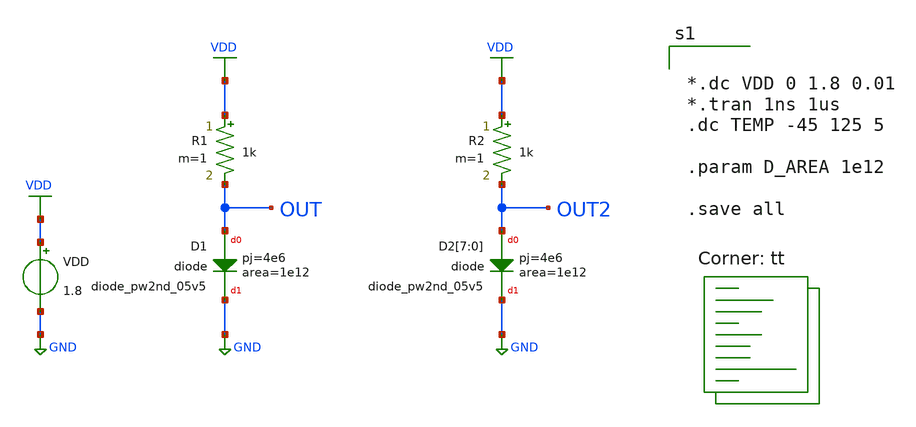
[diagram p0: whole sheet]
** sch_path: design/CNR_GR04_SKY130NM/CNR_GR4_Temp_Sweep_PK.sch
**.subckt CNR_GR4_Temp_Sweep_PK
XD1 OUT GND sky130_fd_pr__diode_pw2nd_05v5 area=1e12 pj=4e6
R1 VDD OUT 1k m=1
VDD VDD GND 1.8
XD2[7] OUT2 GND sky130_fd_pr__diode_pw2nd_05v5 area=1e12 pj=4e6
XD2[6] OUT2 GND sky130_fd_pr__diode_pw2nd_05v5 area=1e12 pj=4e6
XD2[5] OUT2 GND sky130_fd_pr__diode_pw2nd_05v5 area=1e12 pj=4e6
XD2[4] OUT2 GND sky130_fd_pr__diode_pw2nd_05v5 area=1e12 pj=4e6
XD2[3] OUT2 GND sky130_fd_pr__diode_pw2nd_05v5 area=1e12 pj=4e6
XD2[2] OUT2 GND sky130_fd_pr__diode_pw2nd_05v5 area=1e12 pj=4e6
XD2[1] OUT2 GND sky130_fd_pr__diode_pw2nd_05v5 area=1e12 pj=4e6
XD2[0] OUT2 GND sky130_fd_pr__diode_pw2nd_05v5 area=1e12 pj=4e6
R2 VDD OUT2 1k m=1
**** begin user architecture code


*.dc VDD 0 1.8 0.01
*.tran 1ns 1us
.dc TEMP -45 125 5

.param D_AREA 1e12

.save all



.lib $::SKYWATER_MODELS/sky130.lib.spice tt
**** end user architecture code
**.ends
.GLOBAL GND
.GLOBAL VDD
.end
